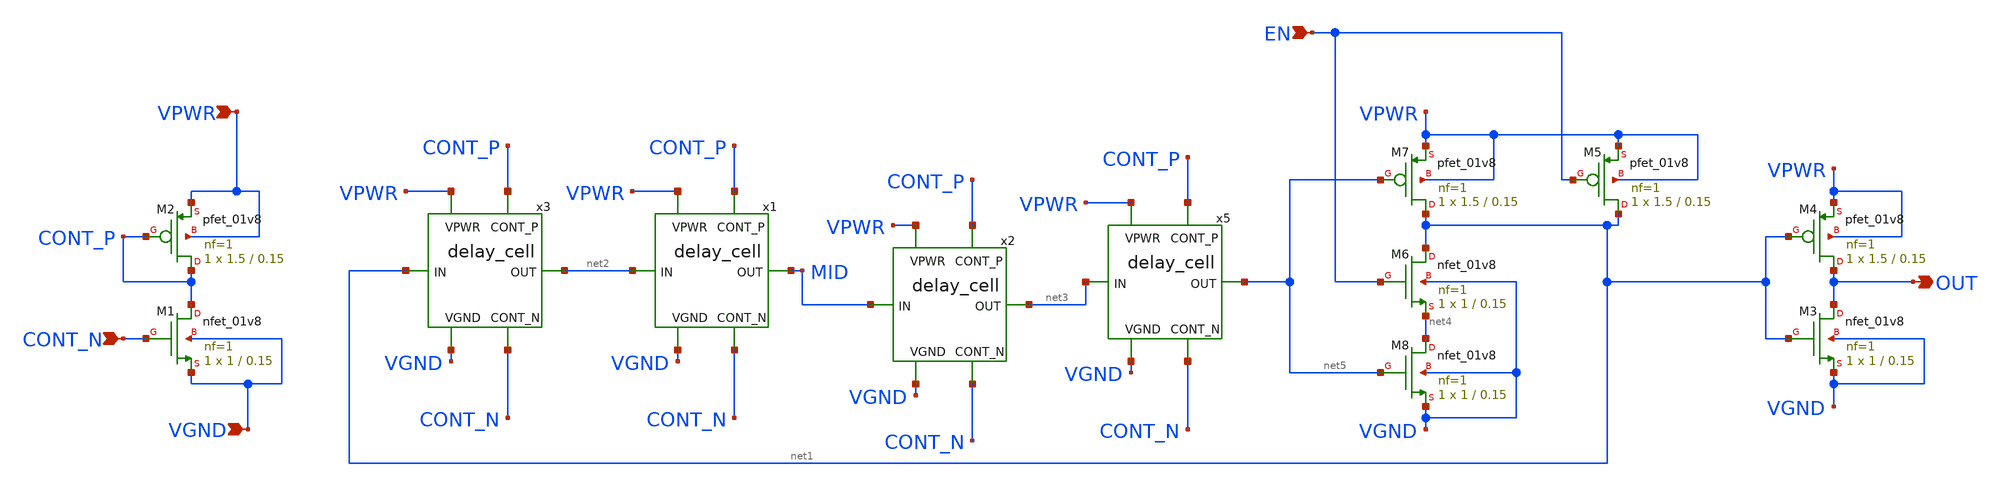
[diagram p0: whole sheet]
** sch_path: xschem/ring_osc/vco.sch
**.subckt vco CONT_N VGND VPWR EN OUT
*.ipin CONT_N
*.ipin VGND
*.ipin VPWR
*.ipin EN
*.opin OUT
x1 VPWR CONT_P net2 MID CONT_N VGND delay_cell
XM1 CONT_P CONT_N VGND VGND sky130_fd_pr__nfet_01v8 L=0.15 W=1 nf=1 ad='int((nf+1)/2) * W/nf * 0.29'
+ as='int((nf+2)/2) * W/nf * 0.29' pd='2*int((nf+1)/2) * (W/nf + 0.29)' ps='2*int((nf+2)/2) * (W/nf + 0.29)'
+ nrd='0.29 / W' nrs='0.29 / W' sa=0 sb=0 sd=0 mult=1 m=1
XM2 CONT_P CONT_P VPWR VPWR sky130_fd_pr__pfet_01v8 L=0.15 W=1.5 nf=1 ad='int((nf+1)/2) * W/nf * 0.29'
+ as='int((nf+2)/2) * W/nf * 0.29' pd='2*int((nf+1)/2) * (W/nf + 0.29)' ps='2*int((nf+2)/2) * (W/nf + 0.29)'
+ nrd='0.29 / W' nrs='0.29 / W' sa=0 sb=0 sd=0 mult=1 m=1
x2 VPWR CONT_P MID net3 CONT_N VGND delay_cell
x3 VPWR CONT_P net1 net2 CONT_N VGND delay_cell
x5 VPWR CONT_P net3 net5 CONT_N VGND delay_cell
XM3 OUT net1 VGND VGND sky130_fd_pr__nfet_01v8 L=0.15 W=1 nf=1 ad='int((nf+1)/2) * W/nf * 0.29' as='int((nf+2)/2) * W/nf * 0.29'
+ pd='2*int((nf+1)/2) * (W/nf + 0.29)' ps='2*int((nf+2)/2) * (W/nf + 0.29)' nrd='0.29 / W' nrs='0.29 / W'
+ sa=0 sb=0 sd=0 mult=1 m=1
XM4 OUT net1 VPWR VPWR sky130_fd_pr__pfet_01v8 L=0.15 W=1.5 nf=1 ad='int((nf+1)/2) * W/nf * 0.29' as='int((nf+2)/2) * W/nf * 0.29'
+ pd='2*int((nf+1)/2) * (W/nf + 0.29)' ps='2*int((nf+2)/2) * (W/nf + 0.29)' nrd='0.29 / W' nrs='0.29 / W'
+ sa=0 sb=0 sd=0 mult=1 m=1
XM6 net1 EN net4 VGND sky130_fd_pr__nfet_01v8 L=0.15 W=1 nf=1 ad='int((nf+1)/2) * W/nf * 0.29' as='int((nf+2)/2) * W/nf * 0.29'
+ pd='2*int((nf+1)/2) * (W/nf + 0.29)' ps='2*int((nf+2)/2) * (W/nf + 0.29)' nrd='0.29 / W' nrs='0.29 / W'
+ sa=0 sb=0 sd=0 mult=1 m=1
XM7 net1 net5 VPWR VPWR sky130_fd_pr__pfet_01v8 L=0.15 W=1.5 nf=1 ad='int((nf+1)/2) * W/nf * 0.29' as='int((nf+2)/2) * W/nf * 0.29'
+ pd='2*int((nf+1)/2) * (W/nf + 0.29)' ps='2*int((nf+2)/2) * (W/nf + 0.29)' nrd='0.29 / W' nrs='0.29 / W'
+ sa=0 sb=0 sd=0 mult=1 m=1
XM8 net4 net5 VGND VGND sky130_fd_pr__nfet_01v8 L=0.15 W=1 nf=1 ad='int((nf+1)/2) * W/nf * 0.29' as='int((nf+2)/2) * W/nf * 0.29'
+ pd='2*int((nf+1)/2) * (W/nf + 0.29)' ps='2*int((nf+2)/2) * (W/nf + 0.29)' nrd='0.29 / W' nrs='0.29 / W'
+ sa=0 sb=0 sd=0 mult=1 m=1
XM5 net1 EN VPWR VPWR sky130_fd_pr__pfet_01v8 L=0.15 W=1.5 nf=1 ad='int((nf+1)/2) * W/nf * 0.29' as='int((nf+2)/2) * W/nf * 0.29'
+ pd='2*int((nf+1)/2) * (W/nf + 0.29)' ps='2*int((nf+2)/2) * (W/nf + 0.29)' nrd='0.29 / W' nrs='0.29 / W'
+ sa=0 sb=0 sd=0 mult=1 m=1
**.ends

* expanding   symbol:  delay_cell.sym # of pins=6
** sym_path: delay_cell.sym
** sch_path: delay_cell.sch
.subckt delay_cell VPWR CONT_P IN OUT CONT_N VGND
*.ipin VPWR
*.ipin VGND
*.ipin IN
*.ipin CONT_N
*.ipin CONT_P
*.opin OUT
XM1 OUT IN net1 VGND sky130_fd_pr__nfet_01v8 L=0.15 W=1 nf=1 ad='int((nf+1)/2) * W/nf * 0.29' as='int((nf+2)/2) * W/nf * 0.29'
+ pd='2*int((nf+1)/2) * (W/nf + 0.29)' ps='2*int((nf+2)/2) * (W/nf + 0.29)' nrd='0.29 / W' nrs='0.29 / W'
+ sa=0 sb=0 sd=0 mult=1 m=1
XM2 net1 CONT_N VGND VGND sky130_fd_pr__nfet_01v8 L=0.15 W=1 nf=1 ad='int((nf+1)/2) * W/nf * 0.29' as='int((nf+2)/2) * W/nf * 0.29'
+ pd='2*int((nf+1)/2) * (W/nf + 0.29)' ps='2*int((nf+2)/2) * (W/nf + 0.29)' nrd='0.29 / W' nrs='0.29 / W'
+ sa=0 sb=0 sd=0 mult=1 m=1
XM3 OUT IN net2 VPWR sky130_fd_pr__pfet_01v8 L=0.15 W=1 nf=1 ad='int((nf+1)/2) * W/nf * 0.29' as='int((nf+2)/2) * W/nf * 0.29'
+ pd='2*int((nf+1)/2) * (W/nf + 0.29)' ps='2*int((nf+2)/2) * (W/nf + 0.29)' nrd='0.29 / W' nrs='0.29 / W'
+ sa=0 sb=0 sd=0 mult=1 m=1
XM4 net2 CONT_P VPWR VPWR sky130_fd_pr__pfet_01v8 L=0.15 W=1.5 nf=1 ad='int((nf+1)/2) * W/nf * 0.29'
+ as='int((nf+2)/2) * W/nf * 0.29' pd='2*int((nf+1)/2) * (W/nf + 0.29)' ps='2*int((nf+2)/2) * (W/nf + 0.29)'
+ nrd='0.29 / W' nrs='0.29 / W' sa=0 sb=0 sd=0 mult=1 m=1
.ends

.end
